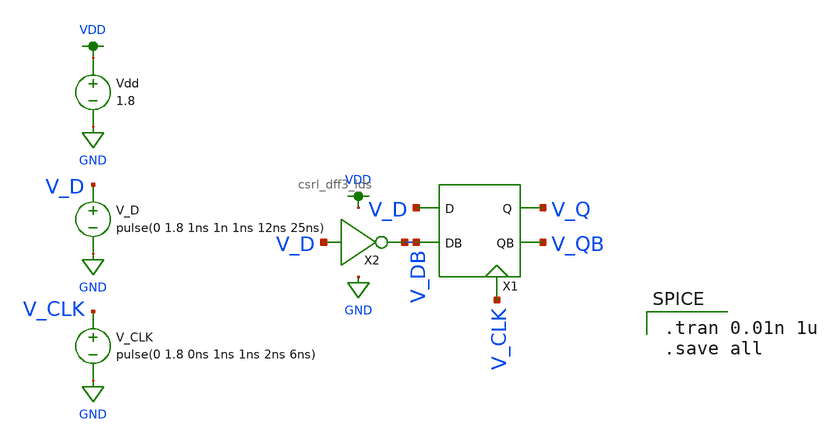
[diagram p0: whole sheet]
** sch_path: simulation/shift_register/lauren_mp2_files/csrl_dff3_tran.sch
**.subckt csrl_dff3_tran
X2 V_D V_DB inverter
Vdd VDD GND 1.8
V_D V_D GND pulse(0 1.8 1ns 1n 1ns 12ns 25ns)
V_CLK V_CLK GND pulse(0 1.8 0ns 1ns 1ns 2ns 6ns)
X1 V_D V_DB V_Q V_QB V_CLK csrl_dff3_lds
**** begin user architecture code

.tran 0.01n 1u
.save all


.option wnflag=1
.lib ~/skywater/skywater-pdk/libraries/sky130_fd_pr_ngspice/latest/models/sky130.lib.spice sf

**** end user architecture code
**.ends
.GLOBAL GND
.GLOBAL VDD
.end
